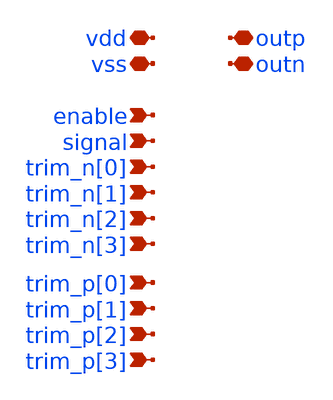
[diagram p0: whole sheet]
** sch_path: xschem/injector_pex.sch
**.subckt injector_pex enable signal trim_n[0] trim_n[1] trim_n[2] trim_n[3] trim_p[0] trim_p[1]
*+ trim_p[2] trim_p[3] vss vdd outp outn
*.ipin enable
*.ipin signal
*.ipin trim_n[0]
*.ipin trim_n[1]
*.ipin trim_n[2]
*.ipin trim_n[3]
*.ipin trim_p[0]
*.ipin trim_p[1]
*.ipin trim_p[2]
*.ipin trim_p[3]
*.iopin vss
*.iopin vdd
*.iopin outp
*.iopin outn
**** begin user architecture code

* NGSPICE file created from injector_flat.ext - technology: gf180mcuC

.subckt injector_flat enable outn outp signal trim_n[0] trim_n[1] trim_n[2] trim_n[3]  trim_p[0]
+ trim_p[1] trim_p[2] trim_p[3] vss vdd
X0 _13_ a_8301_4728# vdd vdd pfet_06v0 w=1.22u l=0.5u
X1 vdd a_9644_7080# a_9556_7124# vdd pfet_06v0 w=1.22u l=1u
X2 a_3055_3728# a_2612_3229# vdd vdd pfet_06v0 w=0.62u l=0.5u
X3 outn _00_ vdd vdd pfet_06v0 w=1.22u l=0.5u
X4 outp _00_ vdd vdd pfet_06v0 w=1.22u l=0.5u
X5 vdd trim_p[0] a_2388_7933# vdd pfet_06v0 w=0.62u l=0.5u
X6 _09_ a_6285_4728# vdd vdd pfet_06v0 w=1.22u l=0.5u
X7 vdd a_3036_5079# a_2948_5176# vdd pfet_06v0 w=1.22u l=1u
X8 outn _00_ vdd vdd pfet_06v0 w=1.22u l=0.5u
X9 a_5948_7080# a_5860_7124# vss vss nfet_06v0 w=0.82u l=1u
X10 outn _00_ vss vss nfet_06v0 w=0.82u l=0.6u
X11 vdd _20_ outp vdd pfet_06v0 w=1.22u l=0.5u
X12 vss trim_p[1] a_7204_7933# vss nfet_06v0 w=0.36u l=0.6u
X13 a_15496_8308# trim_p[3] vdd vdd pfet_06v0 w=0.62u l=0.5u
X14 outp _18_ vdd vdd pfet_06v0 w=1.22u l=0.5u
X15 outp _00_ vdd vdd pfet_06v0 w=1.22u l=0.5u
X16 a_3820_5512# a_3732_5556# vss vss nfet_06v0 w=0.82u l=1u
X17 outp _00_ vdd vdd pfet_06v0 w=1.22u l=0.5u
X18 outn _00_ vdd vdd pfet_06v0 w=1.22u l=0.5u
X19 outp _00_ vdd vdd pfet_06v0 w=1.22u l=0.5u
X20 vdd a_5052_7080# a_4964_7124# vdd pfet_06v0 w=1.22u l=1u
X21 a_8573_7889# _00_ vss vss nfet_06v0 w=0.36u l=0.6u
X22 a_14703_8432# a_15496_8308# a_14723_7933# vdd pfet_06v0 w=0.62u l=0.5u
X23 a_3932_6647# a_3844_6744# vss vss nfet_06v0 w=0.82u l=1u
X24 a_7636_7675# a_7204_7156# vss vss nfet_06v0 w=0.36u l=0.6u
X25 _06_ a_14237_3944# vdd vdd pfet_06v0 w=1.22u l=0.5u
X26 vdd a_3484_5079# a_3396_5176# vdd pfet_06v0 w=1.22u l=1u
X27 outp _00_ vdd vdd pfet_06v0 w=1.22u l=0.5u
X28 outp _00_ vss vss nfet_06v0 w=0.82u l=0.6u
X29 vdd _15_ outn vdd pfet_06v0 w=1.22u l=0.5u
X30 a_9869_3160# a_9869_3160# vss vss nfet_06v0 w=0.82u l=0.6u
X31 a_16280_3604# trim_n[3] vss vss nfet_06v0 w=0.36u l=0.6u
X32 a_6621_3160# a_6621_3160# vss vss nfet_06v0 w=0.82u l=0.6u
X33 outp _00_ vdd vdd pfet_06v0 w=1.22u l=0.5u
X34 vdd _26_ a_11124_3229# vdd pfet_06v0 w=0.62u l=0.5u
X35 vdd a_2140_3944# a_2052_3988# vdd pfet_06v0 w=1.22u l=1u
X36 vdd a_3981_4417# a_3004_4020# vdd pfet_06v0 w=0.62u l=0.5u
X37 outn _00_ vss vss nfet_06v0 w=0.82u l=0.6u
X38 vss signal_n a_2161_6296# vss nfet_06v0 w=0.36u l=0.6u
X39 outn _00_ vss vss nfet_06v0 w=0.82u l=0.6u
X40 outn _00_ vdd vdd pfet_06v0 w=1.22u l=0.5u
X41 outp a_14703_8432# vdd vdd pfet_06v0 w=1.095u l=0.5u
X42 a_16280_3604# trim_n[3] vdd vdd pfet_06v0 w=0.62u l=0.5u
X43 outn a_7555_4539# vss vss nfet_06v0 w=0.82u l=0.6u
X44 a_16700_3944# a_16612_3988# vss vss nfet_06v0 w=0.82u l=1u
X45 vdd a_2140_5079# a_2052_5176# vdd pfet_06v0 w=1.22u l=1u
X46 vss a_3757_7889# a_2820_7933# vss nfet_06v0 w=0.36u l=0.6u
X47 outp _00_ vss vss nfet_06v0 w=0.82u l=0.6u
X48 vdd a_8573_7553# a_7596_7156# vdd pfet_06v0 w=0.62u l=0.5u
X49 a_16851_4797# a_16388_4797# vss vss nfet_06v0 w=0.36u l=0.6u
X50 outp _00_ vdd vdd pfet_06v0 w=1.22u l=0.5u
X51 a_15487_3728# a_16280_3604# a_15507_3229# vdd pfet_06v0 w=0.62u l=0.5u
X52 outn _00_ vdd vdd pfet_06v0 w=1.22u l=0.5u
X53 vdd a_3004_4020# outn vdd pfet_06v0 w=1.095u l=0.5u
X54 a_12463_3988# a_12020_4539# vdd vdd pfet_06v0 w=0.62u l=0.5u
X55 outp _00_ vss vss nfet_06v0 w=0.82u l=0.6u
X56 vdd a_4828_6647# a_4740_6744# vdd pfet_06v0 w=1.22u l=1u
X57 vss _22_ a_2612_3229# vss nfet_06v0 w=0.36u l=0.6u
X58 vss signal a_1924_6040# vss nfet_06v0 w=0.365u l=0.6u
X59 vss _07_ outn vss nfet_06v0 w=0.82u l=0.6u
X60 a_12360_8308# trim_p[2] vss vss nfet_06v0 w=0.36u l=0.6u
X61 _10_ a_10093_3944# vdd vdd pfet_06v0 w=1.22u l=0.5u
X62 vdd a_6060_8215# a_5972_8312# vdd pfet_06v0 w=1.22u l=1u
X63 _03_ a_1716_6040# vdd vdd pfet_06v0 w=1.215u l=0.5u
X64 a_12780_5079# a_12692_5176# vss vss nfet_06v0 w=0.82u l=1u
X65 vdd a_17932_8215# a_17844_8312# vdd pfet_06v0 w=1.22u l=1u
X66 _03_ a_1716_6040# vss vss nfet_06v0 w=0.815u l=0.6u
X67 vdd a_8573_7889# a_7596_8400# vdd pfet_06v0 w=0.62u l=0.5u
X68 a_7667_3229# trim_n[1] a_7647_3728# vss nfet_06v0 w=0.36u l=0.6u
X69 a_10541_3160# a_10541_3160# vss vss nfet_06v0 w=0.82u l=0.6u
X70 a_4268_5512# a_4180_5556# vss vss nfet_06v0 w=0.82u l=1u
X71 outn _09_ vss vss nfet_06v0 w=0.82u l=0.6u
X72 a_12483_4539# a_12020_4539# vss vss nfet_06v0 w=0.36u l=0.6u
X73 a_7667_3229# a_7204_3229# vss vss nfet_06v0 w=0.36u l=0.6u
X74 vss _25_ a_12020_4539# vss nfet_06v0 w=0.36u l=0.6u
X75 a_3004_4020# trim_n[0] vdd vdd pfet_06v0 w=0.62u l=0.5u
X76 a_1692_6647# a_1604_6744# vss vss nfet_06v0 w=0.82u l=1u
X77 vss trim_p[2] a_12020_7156# vss nfet_06v0 w=0.36u l=0.6u
X78 vss a_16280_3604# a_15507_3229# vss nfet_06v0 w=0.36u l=0.6u
X79 a_3055_3728# a_3848_3604# a_3075_3229# vdd pfet_06v0 w=0.62u l=0.5u
X80 _28_ a_5501_5512# vdd vdd pfet_06v0 w=1.22u l=0.5u
X81 vss _00_ outn vss nfet_06v0 w=0.82u l=0.6u
X82 a_8189_5512# a_8189_5512# vss vss nfet_06v0 w=0.82u l=0.6u
X83 a_3757_7889# _00_ vss vss nfet_06v0 w=0.36u l=0.6u
X84 outn _00_ vss vss nfet_06v0 w=0.82u l=0.6u
X85 a_8573_7553# _00_ vdd vdd pfet_06v0 w=0.62u l=0.5u
X86 a_2161_6296# _00_ vss vss nfet_06v0 w=0.36u l=0.6u
X87 outn a_14835_7675# vss vss nfet_06v0 w=0.82u l=0.6u
X88 a_6844_7080# a_6756_7124# vss vss nfet_06v0 w=0.82u l=1u
X89 vdd a_9644_3944# a_9556_3988# vdd pfet_06v0 w=1.22u l=1u
X90 vdd a_4716_5512# a_4628_5556# vdd pfet_06v0 w=1.22u l=1u
X91 a_5612_6647# a_5524_6744# vss vss nfet_06v0 w=0.82u l=1u
X92 a_14815_7124# a_15608_7112# a_14835_7675# vdd pfet_06v0 w=0.62u l=0.5u
X93 a_7596_7156# trim_p[1] a_7636_7675# vss nfet_06v0 w=0.36u l=0.6u
X94 vss _00_ outn vss nfet_06v0 w=0.82u l=0.6u
X95 vdd a_3932_6647# a_3844_6744# vdd pfet_06v0 w=1.22u l=1u
X96 vss a_2820_7675# outp vss nfet_06v0 w=0.82u l=0.6u
X97 vdd trim_n[1] a_7535_3988# vdd pfet_06v0 w=0.62u l=0.5u
X98 vdd signal a_1716_6040# vdd pfet_06v0 w=0.6u l=0.5u
X99 a_12412_7156# trim_p[2] a_12452_7675# vss nfet_06v0 w=0.36u l=0.6u
X100 _05_ a_9869_3160# vdd vdd pfet_06v0 w=1.22u l=0.5u
X101 _25_ a_6621_3160# vdd vdd pfet_06v0 w=1.22u l=0.5u
X102 a_16831_5296# a_17624_5172# a_16851_4797# vdd pfet_06v0 w=0.62u l=0.5u
X103 vdd a_7596_7156# outn vdd pfet_06v0 w=1.095u l=0.5u
X104 vss a_17699_6040# a_17699_6040# vss nfet_06v0 w=0.82u l=0.6u
X105 vdd trim_n[1] a_7647_3728# vdd pfet_06v0 w=0.62u l=0.5u
X106 a_2780_7156# trim_p[0] vdd vdd pfet_06v0 w=0.62u l=0.5u
X107 vdd _00_ outp vdd pfet_06v0 w=1.22u l=0.5u
X108 vdd a_14012_7080# a_13924_7124# vdd pfet_06v0 w=1.22u l=1u
X109 a_5500_7080# a_5412_7124# vss vss nfet_06v0 w=0.82u l=1u
X110 outp _00_ vss vss nfet_06v0 w=0.82u l=0.6u
X111 a_8573_7889# _00_ vdd vdd pfet_06v0 w=0.62u l=0.5u
X112 vdd a_3296_6296# _02_ vdd pfet_06v0 w=1.22u l=0.5u
X113 a_3372_5512# a_3284_5556# vss vss nfet_06v0 w=0.82u l=1u
X114 vss a_12360_8308# a_11587_7933# vss nfet_06v0 w=0.36u l=0.6u
X115 outn _00_ vss vss nfet_06v0 w=0.82u l=0.6u
X116 a_2820_7933# a_2388_7933# a_2780_8400# vdd pfet_06v0 w=0.62u l=0.5u
X117 a_5612_8215# a_5524_8312# vss vss nfet_06v0 w=0.82u l=1u
X118 a_2161_6296# signal_n a_2553_6875# vdd pfet_06v0 w=0.565u l=0.5u
X119 a_11587_3229# a_11124_3229# vss vss nfet_06v0 w=0.36u l=0.6u
X120 vdd trim_n[0] a_3055_3728# vdd pfet_06v0 w=0.62u l=0.5u
X121 vdd signal signal_n vdd pfet_06v0 w=1.22u l=0.5u
X122 outp _00_ vss vss nfet_06v0 w=0.82u l=0.6u
X123 outn _00_ vdd vdd pfet_06v0 w=1.22u l=0.5u
X124 a_15507_3229# trim_n[3] a_15487_3728# vss nfet_06v0 w=0.36u l=0.6u
X125 vss a_2820_7933# outn vss nfet_06v0 w=0.82u l=0.6u
X126 outp _10_ vss vss nfet_06v0 w=0.82u l=0.6u
X127 vdd a_3820_5512# a_3732_5556# vdd pfet_06v0 w=1.22u l=1u
X128 outp _06_ vdd vdd pfet_06v0 w=1.22u l=0.5u
X129 vdd a_7596_8400# outp vdd pfet_06v0 w=1.095u l=0.5u
X130 a_14237_3160# a_14237_3160# vss vss nfet_06v0 w=0.82u l=0.6u
X131 outp _00_ vdd vdd pfet_06v0 w=1.22u l=0.5u
X132 outp _00_ vss vss nfet_06v0 w=0.82u l=0.6u
X133 a_3296_6296# _03_ vss vss nfet_06v0 w=0.36u l=0.6u
X134 a_16831_5296# a_16388_4797# vdd vdd pfet_06v0 w=0.62u l=0.5u
X135 outn _05_ vss vss nfet_06v0 w=0.82u l=0.6u
X136 vdd a_6947_4772# _11_ vdd pfet_06v0 w=1.22u l=0.5u
X137 outp _12_ vdd vdd pfet_06v0 w=1.22u l=0.5u
X138 outn a_12483_4539# vss vss nfet_06v0 w=0.82u l=0.6u
X139 _16_ a_10541_3160# vdd vdd pfet_06v0 w=1.22u l=0.5u
X140 a_4829_4728# a_4829_4728# vss vss nfet_06v0 w=0.82u l=0.6u
X141 outp _00_ vdd vdd pfet_06v0 w=1.22u l=0.5u
X142 outp _00_ vss vss nfet_06v0 w=0.82u l=0.6u
X143 a_7647_3728# a_7204_3229# vdd vdd pfet_06v0 w=0.62u l=0.5u
X144 outn _00_ vss vss nfet_06v0 w=0.82u l=0.6u
X145 a_12452_7675# a_12020_7156# vss vss nfet_06v0 w=0.36u l=0.6u
X146 vdd trim_n[2] a_11567_3728# vdd pfet_06v0 w=0.62u l=0.5u
X147 vdd a_1692_6647# a_1604_6744# vdd pfet_06v0 w=1.22u l=1u
X148 vdd _00_ outp vdd pfet_06v0 w=1.22u l=0.5u
X149 outp _00_ vdd vdd pfet_06v0 w=1.22u l=0.5u
X150 a_3757_7553# _00_ vdd vdd pfet_06v0 w=0.62u l=0.5u
X151 vdd _07_ outn vdd pfet_06v0 w=1.22u l=0.5u
X152 a_12668_6647# a_12580_6744# vss vss nfet_06v0 w=0.82u l=1u
X153 vdd a_12780_5079# a_12692_5176# vdd pfet_06v0 w=1.22u l=1u
X154 vdd _27_ a_15044_3229# vdd pfet_06v0 w=0.62u l=0.5u
X155 outn _00_ vdd vdd pfet_06v0 w=1.22u l=0.5u
X156 vdd a_16700_3944# a_16612_3988# vdd pfet_06v0 w=1.22u l=1u
X157 vdd a_5612_6647# a_5524_6744# vdd pfet_06v0 w=1.22u l=1u
X158 a_11587_7933# trim_p[2] a_11567_8432# vss nfet_06v0 w=0.36u l=0.6u
X159 a_9644_5512# a_9556_5556# vss vss nfet_06v0 w=0.82u l=1u
X160 outn _00_ vdd vdd pfet_06v0 w=1.22u l=0.5u
X161 outn _00_ vdd vdd pfet_06v0 w=1.22u l=0.5u
X162 a_5837_3944# a_5837_3944# vss vss nfet_06v0 w=0.82u l=0.6u
X163 vss _28_ a_16388_4797# vss nfet_06v0 w=0.36u l=0.6u
X164 a_2780_8400# trim_p[0] a_2820_7933# vss nfet_06v0 w=0.36u l=0.6u
X165 outn _00_ vss vss nfet_06v0 w=0.82u l=0.6u
X166 vdd a_6835_6340# _15_ vdd pfet_06v0 w=1.22u l=0.5u
X167 a_6509_3944# a_6509_3944# vss vss nfet_06v0 w=0.82u l=0.6u
X168 a_3757_7889# _00_ vdd vdd pfet_06v0 w=0.62u l=0.5u
X169 a_1716_6040# enable vdd vdd pfet_06v0 w=0.6u l=0.5u
X170 outp _00_ vss vss nfet_06v0 w=0.82u l=0.6u
X171 outn _00_ vss vss nfet_06v0 w=0.82u l=0.6u
X172 outp _08_ vdd vdd pfet_06v0 w=1.22u l=0.5u
X173 a_16365_5512# a_16365_5512# vss vss nfet_06v0 w=0.82u l=0.6u
X174 a_14723_7933# trim_p[3] a_14703_8432# vss nfet_06v0 w=0.36u l=0.6u
X175 a_6396_7080# a_6308_7124# vss vss nfet_06v0 w=0.82u l=1u
X176 a_11567_3728# a_11124_3229# vdd vdd pfet_06v0 w=0.62u l=0.5u
X177 outp _00_ vss vss nfet_06v0 w=0.82u l=0.6u
X178 a_4640_7864# _04_ vss vss nfet_06v0 w=0.36u l=0.6u
X179 vdd a_4268_5512# a_4180_5556# vdd pfet_06v0 w=1.22u l=1u
X180 a_9644_7080# a_9556_7124# vss vss nfet_06v0 w=0.82u l=1u
X181 vss a_17475_3204# a_17475_3204# vss nfet_06v0 w=0.82u l=0.6u
X182 vss trim_p[1] a_7204_7156# vss nfet_06v0 w=0.36u l=0.6u
X183 a_3981_4417# _21_ vdd vdd pfet_06v0 w=0.62u l=0.5u
X184 outp _00_ vss vss nfet_06v0 w=0.82u l=0.6u
X185 vss a_7636_7675# outn vss nfet_06v0 w=0.82u l=0.6u
X186 vdd trim_n[2] a_12463_3988# vdd pfet_06v0 w=0.62u l=0.5u
X187 outn _17_ vdd vdd pfet_06v0 w=1.22u l=0.5u
X188 outn _17_ vss vss nfet_06v0 w=0.82u l=0.6u
X189 a_8573_7553# _00_ vss vss nfet_06v0 w=0.36u l=0.6u
X190 a_7596_7156# trim_p[1] vdd vdd pfet_06v0 w=0.62u l=0.5u
X191 vdd _00_ outp vdd pfet_06v0 w=1.22u l=0.5u
X192 outn _00_ vss vss nfet_06v0 w=0.82u l=0.6u
X193 vdd _00_ outn vdd pfet_06v0 w=1.22u l=0.5u
X194 _08_ a_8189_5512# vdd vdd pfet_06v0 w=1.22u l=0.5u
X195 a_4380_6647# a_4292_6744# vss vss nfet_06v0 w=0.82u l=1u
X196 _18_ a_14237_3160# vdd vdd pfet_06v0 w=1.22u l=0.5u
X197 outp _16_ vss vss nfet_06v0 w=0.82u l=0.6u
X198 a_12412_7156# trim_p[2] vdd vdd pfet_06v0 w=0.62u l=0.5u
X199 a_5052_7080# a_4964_7124# vss vss nfet_06v0 w=0.82u l=1u
X200 a_15496_8308# trim_p[3] vss vss nfet_06v0 w=0.36u l=0.6u
X201 vss a_2161_6296# _04_ vss nfet_06v0 w=0.82u l=0.6u
X202 a_16812_5512# a_16724_5556# vss vss nfet_06v0 w=0.82u l=1u
X203 outp _00_ vss vss nfet_06v0 w=0.82u l=0.6u
X204 a_13389_7553# _00_ vdd vdd pfet_06v0 w=0.62u l=0.5u
X205 vdd _00_ outn vdd pfet_06v0 w=1.22u l=0.5u
X206 outp _00_ vss vss nfet_06v0 w=0.82u l=0.6u
X207 a_3981_4417# _21_ vss vss nfet_06v0 w=0.36u l=0.6u
X208 a_7636_7933# a_7204_7933# a_7596_8400# vdd pfet_06v0 w=0.62u l=0.5u
X209 a_7535_3988# a_8328_3976# a_7555_4539# vdd pfet_06v0 w=0.62u l=0.5u
X210 outn _00_ vdd vdd pfet_06v0 w=1.22u l=0.5u
X211 outn _00_ vss vss nfet_06v0 w=0.82u l=0.6u
X212 vss _23_ a_7092_4539# vss nfet_06v0 w=0.36u l=0.6u
X213 vdd trim_p[1] a_7204_7933# vdd pfet_06v0 w=0.62u l=0.5u
X214 vdd _00_ a_11124_7933# vdd pfet_06v0 w=0.62u l=0.5u
X215 a_8328_3976# trim_n[1] vss vss nfet_06v0 w=0.36u l=0.6u
X216 vss a_3757_7553# a_2820_7675# vss nfet_06v0 w=0.36u l=0.6u
X217 a_2820_7933# a_2388_7933# vss vss nfet_06v0 w=0.36u l=0.6u
X218 outp _00_ vss vss nfet_06v0 w=0.82u l=0.6u
X219 vdd trim_p[0] a_2388_7156# vdd pfet_06v0 w=0.62u l=0.5u
X220 vdd trim_p[2] a_11567_8432# vdd pfet_06v0 w=0.62u l=0.5u
X221 outn _00_ vdd vdd pfet_06v0 w=1.22u l=0.5u
X222 vss a_7636_7933# outp vss nfet_06v0 w=0.82u l=0.6u
X223 outp _00_ vss vss nfet_06v0 w=0.82u l=0.6u
X224 vdd a_3372_5512# a_3284_5556# vdd pfet_06v0 w=1.22u l=1u
X225 outp a_7647_3728# vdd vdd pfet_06v0 w=1.095u l=0.5u
X226 vss _11_ outn vss nfet_06v0 w=0.82u l=0.6u
X227 vdd a_12668_6647# a_12580_6744# vdd pfet_06v0 w=1.22u l=1u
X228 outp _00_ vdd vdd pfet_06v0 w=1.22u l=0.5u
X229 vss _00_ a_14372_7675# vss nfet_06v0 w=0.36u l=0.6u
X230 _17_ a_4829_4728# vdd vdd pfet_06v0 w=1.22u l=0.5u
X231 _00_ enable vdd vdd pfet_06v0 w=1.22u l=0.5u
X232 outp _00_ vss vss nfet_06v0 w=0.82u l=0.6u
X233 vdd a_15683_4772# _14_ vdd pfet_06v0 w=1.22u l=0.5u
X234 vss _26_ a_11124_3229# vss nfet_06v0 w=0.36u l=0.6u
X235 outp a_7667_3229# vss vss nfet_06v0 w=0.82u l=0.6u
X236 vdd _00_ a_14260_7933# vdd pfet_06v0 w=0.62u l=0.5u
X237 vdd _25_ a_12020_4539# vdd pfet_06v0 w=0.62u l=0.5u
X238 outp a_3055_3728# vdd vdd pfet_06v0 w=1.095u l=0.5u
X239 a_15507_3229# a_15044_3229# vss vss nfet_06v0 w=0.36u l=0.6u
X240 vdd trim_p[3] a_14703_8432# vdd pfet_06v0 w=0.62u l=0.5u
X241 vss a_15496_8308# a_14723_7933# vss nfet_06v0 w=0.36u l=0.6u
X242 outp a_3075_3229# vss vss nfet_06v0 w=0.82u l=0.6u
X243 vss a_8573_7889# a_7636_7933# vss nfet_06v0 w=0.36u l=0.6u
X244 outn _00_ vss vss nfet_06v0 w=0.82u l=0.6u
X245 a_3757_7553# _00_ vss vss nfet_06v0 w=0.36u l=0.6u
X246 vdd _23_ a_7092_4539# vdd pfet_06v0 w=0.62u l=0.5u
X247 outp a_16831_5296# vdd vdd pfet_06v0 w=1.095u l=0.5u
X248 vss trim_p[0] a_2388_7933# vss nfet_06v0 w=0.36u l=0.6u
X249 a_6060_6647# a_5972_6744# vss vss nfet_06v0 w=0.82u l=1u
X250 outp a_11567_3728# vdd vdd pfet_06v0 w=1.095u l=0.5u
X251 a_14684_3511# a_14596_3608# vss vss nfet_06v0 w=0.82u l=1u
X252 vdd a_4380_6647# a_4292_6744# vdd pfet_06v0 w=1.22u l=1u
X253 a_3075_3229# trim_n[0] a_3055_3728# vss nfet_06v0 w=0.36u l=0.6u
X254 a_17932_3511# a_17844_3608# vss vss nfet_06v0 w=0.82u l=1u
X255 a_4604_3944# a_4516_3988# vss vss nfet_06v0 w=0.82u l=1u
X256 vdd trim_n[3] a_15487_3728# vdd pfet_06v0 w=0.62u l=0.5u
X257 outn _13_ vdd vdd pfet_06v0 w=1.22u l=0.5u
X258 vdd a_9644_5512# a_9556_5556# vdd pfet_06v0 w=1.22u l=1u
X259 outn _00_ vss vss nfet_06v0 w=0.82u l=0.6u
X260 outn _00_ vss vss nfet_06v0 w=0.82u l=0.6u
X261 _23_ a_5837_3944# vdd vdd pfet_06v0 w=1.22u l=0.5u
X262 a_11587_7933# a_11124_7933# vss vss nfet_06v0 w=0.36u l=0.6u
X263 outn _19_ vdd vdd pfet_06v0 w=1.22u l=0.5u
X264 outp a_11587_3229# vss vss nfet_06v0 w=0.82u l=0.6u
X265 outn a_15487_3728# vdd vdd pfet_06v0 w=1.095u l=0.5u
X266 vdd a_5948_7080# a_5860_7124# vdd pfet_06v0 w=1.22u l=1u
X267 a_4157_4728# a_4157_4728# vss vss nfet_06v0 w=0.82u l=0.6u
X268 outn _00_ vdd vdd pfet_06v0 w=1.22u l=0.5u
X269 vss a_3981_4417# a_3044_4539# vss nfet_06v0 w=0.36u l=0.6u
X270 vdd a_17699_6040# _20_ vdd pfet_06v0 w=1.22u l=0.5u
X271 _19_ a_6509_3944# vdd vdd pfet_06v0 w=1.22u l=0.5u
X272 outp _18_ vss vss nfet_06v0 w=0.82u l=0.6u
X273 a_14012_7080# a_13924_7124# vss vss nfet_06v0 w=0.82u l=1u
X274 outn _00_ vdd vdd pfet_06v0 w=1.22u l=0.5u
X275 a_6060_8215# a_5972_8312# vss vss nfet_06v0 w=0.82u l=1u
X276 vdd a_3757_7553# a_2780_7156# vdd pfet_06v0 w=0.62u l=0.5u
X277 vss a_3044_4539# outn vss nfet_06v0 w=0.82u l=0.6u
X278 a_17932_8215# a_17844_8312# vss vss nfet_06v0 w=0.82u l=1u
X279 _12_ a_16365_5512# vdd vdd pfet_06v0 w=1.22u l=0.5u
X280 outp _00_ vdd vdd pfet_06v0 w=1.22u l=0.5u
X281 vss signal signal_n vss nfet_06v0 w=0.82u l=0.6u
X282 outn a_11587_7933# vss vss nfet_06v0 w=0.82u l=0.6u
X283 a_14723_7933# a_14260_7933# vss vss nfet_06v0 w=0.36u l=0.6u
X284 a_12463_3988# a_13256_3976# a_12483_4539# vdd pfet_06v0 w=0.62u l=0.5u
X285 vdd _22_ a_2612_3229# vdd pfet_06v0 w=0.62u l=0.5u
X286 a_5165_3944# a_5165_3944# vss vss nfet_06v0 w=0.82u l=0.6u
X287 a_7636_7933# a_7204_7933# vss vss nfet_06v0 w=0.36u l=0.6u
X288 vdd _00_ a_14372_7675# vdd pfet_06v0 w=0.62u l=0.5u
X289 vdd trim_n[0] a_2612_4020# vdd pfet_06v0 w=0.62u l=0.5u
X290 outn _00_ vdd vdd pfet_06v0 w=1.22u l=0.5u
X291 vss a_12452_7675# outp vss nfet_06v0 w=0.82u l=0.6u
X292 vss _24_ a_7204_3229# vss nfet_06v0 w=0.36u l=0.6u
X293 a_2588_5079# a_2500_5176# vss vss nfet_06v0 w=0.82u l=1u
X294 outp _10_ vdd vdd pfet_06v0 w=1.22u l=0.5u
X295 a_7555_4539# trim_n[1] a_7535_3988# vss nfet_06v0 w=0.36u l=0.6u
X296 a_15487_3728# a_15044_3229# vdd vdd pfet_06v0 w=0.62u l=0.5u
X297 outn _00_ vdd vdd pfet_06v0 w=1.22u l=0.5u
X298 a_13389_7553# _00_ vss vss nfet_06v0 w=0.36u l=0.6u
X299 outn a_11567_8432# vdd vdd pfet_06v0 w=1.095u l=0.5u
X300 a_13256_3976# trim_n[2] vss vss nfet_06v0 w=0.36u l=0.6u
X301 a_8440_3604# trim_n[1] vss vss nfet_06v0 w=0.36u l=0.6u
X302 a_1692_3944# a_1604_3988# vss vss nfet_06v0 w=0.82u l=1u
X303 vdd trim_p[2] a_12020_7156# vdd pfet_06v0 w=0.62u l=0.5u
X304 outn _00_ vss vss nfet_06v0 w=0.82u l=0.6u
X305 vdd a_3757_7889# a_2780_8400# vdd pfet_06v0 w=0.62u l=0.5u
X306 a_8328_3976# trim_n[1] vdd vdd pfet_06v0 w=0.62u l=0.5u
X307 vdd a_16812_5512# a_16724_5556# vdd pfet_06v0 w=1.22u l=1u
X308 outp _00_ vdd vdd pfet_06v0 w=1.22u l=0.5u
X309 vss a_6947_4772# a_6947_4772# vss nfet_06v0 w=0.82u l=0.6u
X310 outn _00_ vss vss nfet_06v0 w=0.82u l=0.6u
X311 a_4829_3160# a_4829_3160# vss vss nfet_06v0 w=0.82u l=0.6u
X312 vdd trim_n[3] a_16831_5296# vdd pfet_06v0 w=0.62u l=0.5u
X313 a_8440_3604# trim_n[1] vdd vdd pfet_06v0 w=0.62u l=0.5u
X314 a_2820_7675# a_2388_7156# a_2780_7156# vdd pfet_06v0 w=0.62u l=0.5u
X315 vss _14_ outp vss nfet_06v0 w=0.82u l=0.6u
X316 a_3848_3604# trim_n[0] vss vss nfet_06v0 w=0.36u l=0.6u
X317 vss a_17624_5172# a_16851_4797# vss nfet_06v0 w=0.36u l=0.6u
X318 a_14835_7675# trim_p[3] a_14815_7124# vss nfet_06v0 w=0.36u l=0.6u
X319 outp _06_ vss vss nfet_06v0 w=0.82u l=0.6u
X320 vss _00_ outp vss nfet_06v0 w=0.82u l=0.6u
X321 outn _00_ vss vss nfet_06v0 w=0.82u l=0.6u
X322 vdd a_6060_6647# a_5972_6744# vdd pfet_06v0 w=1.22u l=1u
X323 vdd a_14684_3511# a_14596_3608# vdd pfet_06v0 w=1.22u l=1u
X324 a_7647_3728# a_8440_3604# a_7667_3229# vdd pfet_06v0 w=0.62u l=0.5u
X325 vdd a_17932_3511# a_17844_3608# vdd pfet_06v0 w=1.22u l=1u
X326 vdd _11_ outn vdd pfet_06v0 w=1.22u l=0.5u
X327 outp _08_ vss vss nfet_06v0 w=0.82u l=0.6u
X328 a_3044_4539# a_2612_4020# vss vss nfet_06v0 w=0.36u l=0.6u
X329 a_2780_7156# trim_p[0] a_2820_7675# vss nfet_06v0 w=0.36u l=0.6u
X330 vdd a_5612_8215# a_5524_8312# vdd pfet_06v0 w=1.22u l=1u
X331 a_3848_3604# trim_n[0] vdd vdd pfet_06v0 w=0.62u l=0.5u
X332 outp _12_ vss vss nfet_06v0 w=0.82u l=0.6u
X333 a_14815_7124# a_14372_7675# vdd vdd pfet_06v0 w=0.62u l=0.5u
X334 a_2780_8400# trim_p[0] vdd vdd pfet_06v0 w=0.62u l=0.5u
X335 a_1692_5079# a_1604_5176# vss vss nfet_06v0 w=0.82u l=1u
X336 a_2553_6875# _00_ vdd vdd pfet_06v0 w=0.565u l=0.5u
X337 outp _00_ vss vss nfet_06v0 w=0.82u l=0.6u
X338 a_15608_7112# trim_p[3] vss vss nfet_06v0 w=0.36u l=0.6u
X339 vdd a_2780_7156# outp vdd pfet_06v0 w=1.095u l=0.5u
X340 a_5949_3160# a_5949_3160# vss vss nfet_06v0 w=0.82u l=0.6u
X341 a_12360_3604# trim_n[2] vss vss nfet_06v0 w=0.36u l=0.6u
X342 outn a_7535_3988# vdd vdd pfet_06v0 w=1.095u l=0.5u
X343 a_15608_7112# trim_p[3] vdd vdd pfet_06v0 w=0.62u l=0.5u
X344 outp a_16851_4797# vss vss nfet_06v0 w=0.82u l=0.6u
X345 a_1924_6040# enable a_1716_6040# vss nfet_06v0 w=0.365u l=0.6u
X346 outp _00_ vdd vdd pfet_06v0 w=1.22u l=0.5u
X347 outn _00_ vss vss nfet_06v0 w=0.82u l=0.6u
X348 a_5612_5079# a_5524_5176# vss vss nfet_06v0 w=0.82u l=1u
X349 vdd a_6844_7080# a_6756_7124# vdd pfet_06v0 w=1.22u l=1u
X350 vss a_13256_3976# a_12483_4539# vss nfet_06v0 w=0.36u l=0.6u
X351 vss a_8440_3604# a_7667_3229# vss nfet_06v0 w=0.36u l=0.6u
X352 vss _27_ a_15044_3229# vss nfet_06v0 w=0.36u l=0.6u
X353 a_17624_5172# trim_n[3] vdd vdd pfet_06v0 w=0.62u l=0.5u
X354 outn _00_ vdd vdd pfet_06v0 w=1.22u l=0.5u
X355 a_8301_4728# a_8301_4728# vss vss nfet_06v0 w=0.82u l=0.6u
X356 a_14237_3944# a_14237_3944# vss vss nfet_06v0 w=0.82u l=0.6u
X357 a_11567_8432# a_11124_7933# vdd vdd pfet_06v0 w=0.62u l=0.5u
X358 vss _15_ outn vss nfet_06v0 w=0.82u l=0.6u
X359 a_12360_3604# trim_n[2] vdd vdd pfet_06v0 w=0.62u l=0.5u
X360 a_6285_4728# a_6285_4728# vss vss nfet_06v0 w=0.82u l=0.6u
X361 a_3036_5079# a_2948_5176# vss vss nfet_06v0 w=0.82u l=1u
X362 outp _00_ vdd vdd pfet_06v0 w=1.22u l=0.5u
X363 outn _09_ vdd vdd pfet_06v0 w=1.22u l=0.5u
X364 outp _01_ vdd vdd pfet_06v0 w=1.22u l=0.5u
X365 a_2140_3944# a_2052_3988# vss vss nfet_06v0 w=0.82u l=1u
X366 vss _00_ outp vss nfet_06v0 w=0.82u l=0.6u
X367 vss a_6835_6340# a_6835_6340# vss nfet_06v0 w=0.82u l=0.6u
X368 a_7596_8400# trim_p[1] a_7636_7933# vss nfet_06v0 w=0.36u l=0.6u
X369 _21_ a_4157_4728# vdd vdd pfet_06v0 w=1.22u l=0.5u
X370 vdd a_2780_8400# outn vdd pfet_06v0 w=1.095u l=0.5u
X371 outp _00_ vdd vdd pfet_06v0 w=1.22u l=0.5u
X372 a_11567_3728# a_12360_3604# a_11587_3229# vdd pfet_06v0 w=0.62u l=0.5u
X373 vss a_3848_3604# a_3075_3229# vss nfet_06v0 w=0.36u l=0.6u
X374 a_16851_4797# trim_n[3] a_16831_5296# vss nfet_06v0 w=0.36u l=0.6u
X375 vss a_8328_3976# a_7555_4539# vss nfet_06v0 w=0.36u l=0.6u
X376 vdd a_5500_7080# a_5412_7124# vdd pfet_06v0 w=1.22u l=1u
X377 outn _00_ vdd vdd pfet_06v0 w=1.22u l=0.5u
X378 a_2029_3160# a_2029_3160# vss vss nfet_06v0 w=0.82u l=0.6u
X379 outn _02_ vdd vdd pfet_06v0 w=1.22u l=0.5u
X380 outn _02_ vss vss nfet_06v0 w=0.82u l=0.6u
X381 vdd a_4604_3944# a_4516_3988# vdd pfet_06v0 w=1.22u l=1u
X382 outp _00_ vss vss nfet_06v0 w=0.82u l=0.6u
X383 vss trim_n[0] a_2612_4020# vss nfet_06v0 w=0.36u l=0.6u
X384 outn _00_ vss vss nfet_06v0 w=0.82u l=0.6u
X385 a_3484_5079# a_3396_5176# vss vss nfet_06v0 w=0.82u l=1u
X386 a_2820_7675# a_2388_7156# vss vss nfet_06v0 w=0.36u l=0.6u
X387 _00_ enable vss vss nfet_06v0 w=0.82u l=0.6u
X388 vdd a_13389_7553# a_12412_7156# vdd pfet_06v0 w=0.62u l=0.5u
X389 vdd a_4640_7864# _01_ vdd pfet_06v0 w=1.22u l=0.5u
X390 outp _00_ vdd vdd pfet_06v0 w=1.22u l=0.5u
X391 a_3075_3229# a_2612_3229# vss vss nfet_06v0 w=0.36u l=0.6u
X392 _24_ a_4829_3160# vdd vdd pfet_06v0 w=1.22u l=0.5u
X393 a_14703_8432# a_14260_7933# vdd vdd pfet_06v0 w=0.62u l=0.5u
X394 outn _00_ vdd vdd pfet_06v0 w=1.22u l=0.5u
X395 vss _20_ outp vss nfet_06v0 w=0.82u l=0.6u
X396 vss _00_ a_11124_7933# vss nfet_06v0 w=0.36u l=0.6u
X397 a_3296_6296# _03_ vdd vdd pfet_06v0 w=0.565u l=0.5u
X398 vss a_15608_7112# a_14835_7675# vss nfet_06v0 w=0.36u l=0.6u
X399 vdd a_2588_5079# a_2500_5176# vdd pfet_06v0 w=1.22u l=1u
X400 a_10093_3944# a_10093_3944# vss vss nfet_06v0 w=0.82u l=0.6u
X401 vss a_12360_3604# a_11587_3229# vss nfet_06v0 w=0.36u l=0.6u
X402 outn a_15507_3229# vss vss nfet_06v0 w=0.82u l=0.6u
X403 vdd a_12412_7156# outp vdd pfet_06v0 w=1.095u l=0.5u
X404 a_12483_4539# trim_n[2] a_12463_3988# vss nfet_06v0 w=0.36u l=0.6u
X405 a_2140_5079# a_2052_5176# vss vss nfet_06v0 w=0.82u l=1u
X406 a_7535_3988# a_7092_4539# vdd vdd pfet_06v0 w=0.62u l=0.5u
X407 a_13256_3976# trim_n[2] vdd vdd pfet_06v0 w=0.62u l=0.5u
X408 vss a_15683_4772# a_15683_4772# vss nfet_06v0 w=0.82u l=0.6u
X409 outp _01_ vss vss nfet_06v0 w=0.82u l=0.6u
X410 _27_ a_5165_3944# vdd vdd pfet_06v0 w=1.22u l=0.5u
X411 vdd _14_ outp vdd pfet_06v0 w=1.22u l=0.5u
X412 a_5501_5512# a_5501_5512# vss vss nfet_06v0 w=0.82u l=0.6u
X413 a_7636_7675# a_7204_7156# a_7596_7156# vdd pfet_06v0 w=0.62u l=0.5u
X414 vss _00_ a_14260_7933# vss nfet_06v0 w=0.36u l=0.6u
X415 vss _00_ outp vss nfet_06v0 w=0.82u l=0.6u
X416 a_12452_7675# a_12020_7156# a_12412_7156# vdd pfet_06v0 w=0.62u l=0.5u
X417 _26_ a_5949_3160# vdd vdd pfet_06v0 w=1.22u l=0.5u
X418 vdd trim_p[1] a_7204_7156# vdd pfet_06v0 w=0.62u l=0.5u
X419 vss a_8573_7553# a_7636_7675# vss nfet_06v0 w=0.36u l=0.6u
X420 vss a_3296_6296# _02_ vss nfet_06v0 w=0.82u l=0.6u
X421 vdd a_1692_3944# a_1604_3988# vdd pfet_06v0 w=1.22u l=1u
X422 vss a_13389_7553# a_12452_7675# vss nfet_06v0 w=0.36u l=0.6u
X423 a_9644_3944# a_9556_3988# vss vss nfet_06v0 w=0.82u l=1u
X424 a_4716_5512# a_4628_5556# vss vss nfet_06v0 w=0.82u l=1u
X425 a_7555_4539# a_7092_4539# vss vss nfet_06v0 w=0.36u l=0.6u
X426 vdd _28_ a_16388_4797# vdd pfet_06v0 w=0.62u l=0.5u
X427 vdd trim_p[3] a_14815_7124# vdd pfet_06v0 w=0.62u l=0.5u
X428 vss trim_p[0] a_2388_7156# vss nfet_06v0 w=0.36u l=0.6u
X429 outn _05_ vdd vdd pfet_06v0 w=1.22u l=0.5u
X430 a_7596_8400# trim_p[1] vdd vdd pfet_06v0 w=0.62u l=0.5u
X431 vss a_4640_7864# _01_ vss nfet_06v0 w=0.82u l=0.6u
X432 outn _19_ vss vss nfet_06v0 w=0.82u l=0.6u
X433 vdd a_17475_3204# _07_ vdd pfet_06v0 w=1.22u l=0.5u
X434 a_17624_5172# trim_n[3] vss vss nfet_06v0 w=0.36u l=0.6u
X435 vdd a_1692_5079# a_1604_5176# vdd pfet_06v0 w=1.22u l=1u
X436 a_4828_6647# a_4740_6744# vss vss nfet_06v0 w=0.82u l=1u
X437 a_12360_8308# trim_p[2] vdd vdd pfet_06v0 w=0.62u l=0.5u
X438 outn a_14815_7124# vdd vdd pfet_06v0 w=1.095u l=0.5u
X439 vdd _24_ a_7204_3229# vdd pfet_06v0 w=0.62u l=0.5u
X440 outp a_14723_7933# vss vss nfet_06v0 w=0.82u l=0.6u
X441 a_3004_4020# trim_n[0] a_3044_4539# vss nfet_06v0 w=0.36u l=0.6u
X442 a_4640_7864# _04_ vdd vdd pfet_06v0 w=0.565u l=0.5u
X443 a_11567_8432# a_12360_8308# a_11587_7933# vdd pfet_06v0 w=0.62u l=0.5u
X444 _22_ a_2029_3160# vdd vdd pfet_06v0 w=1.22u l=0.5u
X445 outp _16_ vdd vdd pfet_06v0 w=1.22u l=0.5u
X446 outn a_12463_3988# vdd vdd pfet_06v0 w=1.095u l=0.5u
X447 outn _13_ vss vss nfet_06v0 w=0.82u l=0.6u
X448 vdd a_5612_5079# a_5524_5176# vdd pfet_06v0 w=1.22u l=1u
X449 a_14835_7675# a_14372_7675# vss vss nfet_06v0 w=0.36u l=0.6u
X450 a_11587_3229# trim_n[2] a_11567_3728# vss nfet_06v0 w=0.36u l=0.6u
X451 a_3044_4539# a_2612_4020# a_3004_4020# vdd pfet_06v0 w=0.62u l=0.5u
X452 vdd a_2161_6296# _04_ vdd pfet_06v0 w=1.22u l=0.5u
X453 vdd a_6396_7080# a_6308_7124# vdd pfet_06v0 w=1.22u l=1u
C0 _27_ _07_ 2.90fF
C1 outp vdd 5.81fF
C2 _10_ _19_ 3.02fF
C3 outn vdd 5.93fF
C4 _00_ vdd 3.45fF
C5 _00_ _17_ 2.81fF
C6 _08_ outn 3.45fF
C7 outp outn 5.06fF
C8 _00_ outp 6.12fF
C9 _28_ outn 2.17fF
C10 _00_ _28_ 2.35fF
C11 _16_ _00_ 2.42fF
C12 _00_ outn 6.24fF
C13 trim_n[2] vss 2.73fF
C14 trim_n[1] vss 2.75fF
C15 trim_n[0] vss 2.69fF
C16 trim_n[3] vss 2.90fF
C17 trim_p[3] vss 2.63fF
C18 trim_p[2] vss 2.71fF
C19 trim_p[1] vss 2.58fF
C20 outn vss 7.10fF
C21 trim_p[0] vss 2.57fF
C22 outp vss 7.76fF
C23 vdd vss 178.33fF
C24 _00_ vss 22.42fF $ **FLOATING
.ends



XDUT enable outn outp signal trim_n[0] trim_n[1] trim_n[2] trim_n[3]  trim_p[0] trim_p[1] trim_p[2]
+ trim_p[3] vss vdd injector_flat


**** end user architecture code
**.ends
.end
